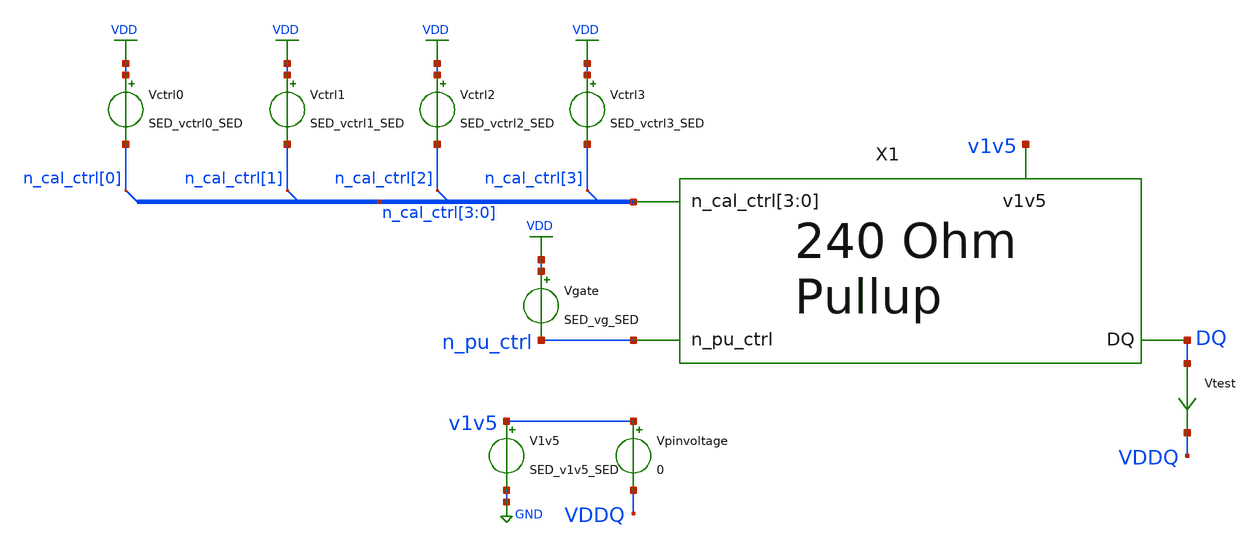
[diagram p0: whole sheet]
** sch_path: p-leg_tb.sch
* Copyright 2021 Stefan Frederik Schippers
* Licensed under the Apache License, Version 2.0 (the "License");
* you may not use this file except in compliance with the License.
* You may obtain a copy of the License at
* https://www.apache.org/licenses/LICENSE-2.0
* Unless required by applicable law or agreed to in writing, software
* distributed under the License is distributed on an "AS IS" BASIS,
* WITHOUT WARRANTIES OR CONDITIONS OF ANY KIND, either express or implied.
* See the License for the specific language governing permissions and
* limitations under the License.
**.subckt p-leg_tb
Vctrl0 VDD n_cal_ctrl[0] SED_vctrl0_SED
Vctrl1 VDD n_cal_ctrl[1] SED_vctrl1_SED
Vctrl2 VDD n_cal_ctrl[2] SED_vctrl2_SED
Vctrl3 VDD n_cal_ctrl[3] SED_vctrl3_SED
Vgate VDD n_pu_ctrl SED_vg_SED
Vtest DQ VDDQ 0
.save i(vtest)
V1v5 v1v5 GND SED_v1v5_SED
Vpinvoltage v1v5 VDDQ 0
X1 DQ v1v5 n_pu_ctrl n_cal_ctrl[3] n_cal_ctrl[2] n_cal_ctrl[1] n_cal_ctrl[0] p-leg
**** begin user architecture code
 ** Local library links to pdk
.lib ./libs/SED_process_SED_lib.spice SED_process_SED

**** end user architecture code
**.ends

* expanding   symbol:  p-leg.sym # of pins=4
** sym_path: p-leg.sym
** sch_path: p-leg.sch
.subckt p-leg DQ v1v5 n_pu_ctrl n_cal_ctrl[3] n_cal_ctrl[2] n_cal_ctrl[1] n_cal_ctrl[0]
*.ipin n_cal_ctrl[3],n_cal_ctrl[2],n_cal_ctrl[1],n_cal_ctrl[0]
*.ipin n_pu_ctrl
*.iopin DQ
*.ipin v1v5
XR1 DQ net1 sky130_fd_pr__res_generic_po W=0.33 L=1.8 m=1
XMpullup net1 n_pu_ctrl v1v5 VDD sky130_fd_pr__pfet_01v8_lvt L=0.35 W=1 nf=1 ad='int((nf+1)/2) * W/nf * 0.29'
+ as='int((nf+2)/2) * W/nf * 0.29' pd='2*int((nf+1)/2) * (W/nf + 0.29)' ps='2*int((nf+2)/2) * (W/nf + 0.29)'
+ nrd='0.29 / W' nrs='0.29 / W' sa=0 sb=0 sd=0 mult=128 m=128
XMctrltot VDD n_cal_ctrl[0] VDD VDD sky130_fd_pr__pfet_01v8_lvt L=0.35 W=1 nf=1 ad='int((nf+1)/2) * W/nf * 0.29'
+ as='int((nf+2)/2) * W/nf * 0.29' pd='2*int((nf+1)/2) * (W/nf + 0.29)' ps='2*int((nf+2)/2) * (W/nf + 0.29)'
+ nrd='0.29 / W' nrs='0.29 / W' sa=0 sb=0 sd=0 mult=120 m=120
XMctrl0 DQ n_cal_ctrl[0] net1 VDD sky130_fd_pr__pfet_01v8_lvt L=0.35 W=1 nf=1 ad='int((nf+1)/2) * W/nf * 0.29'
+ as='int((nf+2)/2) * W/nf * 0.29' pd='2*int((nf+1)/2) * (W/nf + 0.29)' ps='2*int((nf+2)/2) * (W/nf + 0.29)'
+ nrd='0.29 / W' nrs='0.29 / W' sa=0 sb=0 sd=0 mult=64 m=64
XMctrl1 DQ n_cal_ctrl[1] net1 VDD sky130_fd_pr__pfet_01v8_lvt L=0.35 W=1 nf=1 ad='int((nf+1)/2) * W/nf * 0.29'
+ as='int((nf+2)/2) * W/nf * 0.29' pd='2*int((nf+1)/2) * (W/nf + 0.29)' ps='2*int((nf+2)/2) * (W/nf + 0.29)'
+ nrd='0.29 / W' nrs='0.29 / W' sa=0 sb=0 sd=0 mult=16 m=16
XMctrl2 DQ n_cal_ctrl[2] net1 VDD sky130_fd_pr__pfet_01v8_lvt L=0.35 W=1 nf=1 ad='int((nf+1)/2) * W/nf * 0.29'
+ as='int((nf+2)/2) * W/nf * 0.29' pd='2*int((nf+1)/2) * (W/nf + 0.29)' ps='2*int((nf+2)/2) * (W/nf + 0.29)'
+ nrd='0.29 / W' nrs='0.29 / W' sa=0 sb=0 sd=0 mult=8 m=8
XMctrl3 DQ n_cal_ctrl[3] net1 VDD sky130_fd_pr__pfet_01v8_lvt L=0.35 W=1 nf=1 ad='int((nf+1)/2) * W/nf * 0.29'
+ as='int((nf+2)/2) * W/nf * 0.29' pd='2*int((nf+1)/2) * (W/nf + 0.29)' ps='2*int((nf+2)/2) * (W/nf + 0.29)'
+ nrd='0.29 / W' nrs='0.29 / W' sa=0 sb=0 sd=0 mult=4 m=4
.ends

.GLOBAL VDD
.GLOBAL GND
**** begin user architecture code



* power voltage
vvdd VDD 0 1.8

.control
save all
set temp=SED_temp_SED

* RUN SIMULATION
dc Vpinvoltage 0.3 1.2 0.05
* OUTPUT
print (SED_v1v5_SED-vddq)/i(vtest)
wrdata out/data/SED_plotName_SED.txt (SED_v1v5_SED-vddq)/i(vtest)
set hcopydevtype = svg
hardcopy ./out/plots/SED_plotName_SED.svg (SED_v1v5_SED-vddq)/I(vtest) vs vddq title 'Resistance vs pin voltage'

.endc


**** end user architecture code
.end
